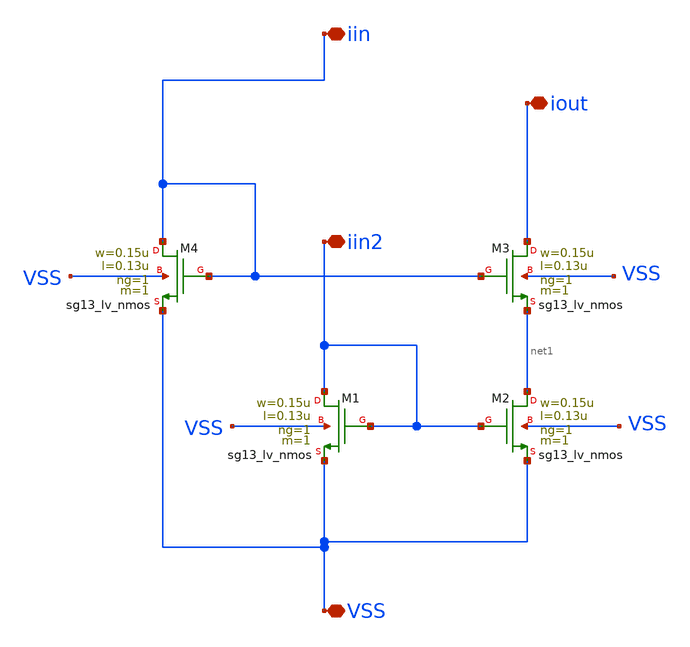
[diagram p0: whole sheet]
** sch_path: analog-db/templates/current_mirror/nmos_current_sink/high_swing_cascode_current_mirror.sch
**.subckt high_swing_cascode_current_mirror VSS iin iout iin2
*.iopin VSS
*.iopin iin
*.iopin iout
*.iopin iin2
XM1 iin2 iin2 VSS VSS sg13_lv_nmos w=0.15u l=0.13u ng=1 m=1 mm_ok=1
XM2 net1 iin2 VSS VSS sg13_lv_nmos w=0.15u l=0.13u ng=1 m=1 mm_ok=1
XM3 iout iin net1 VSS sg13_lv_nmos w=0.15u l=0.13u ng=1 m=1 mm_ok=1
XM4 iin iin VSS VSS sg13_lv_nmos w=0.15u l=0.13u ng=1 m=1 mm_ok=1
**.ends
.end
